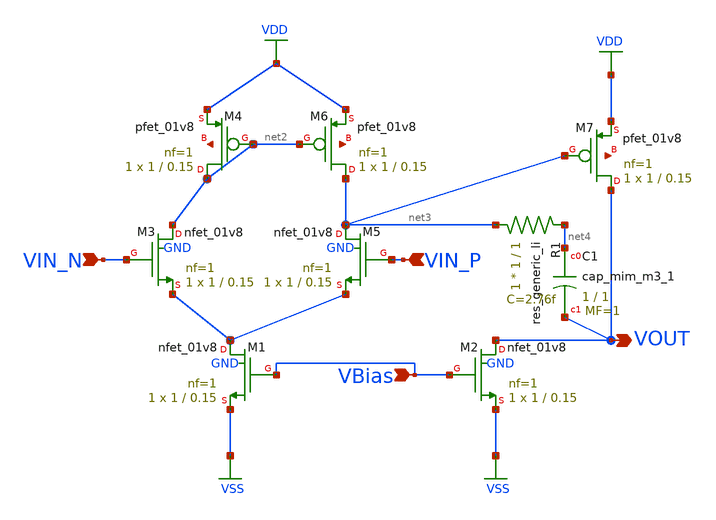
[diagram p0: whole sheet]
** sch_path: analog/schematics/bootcamp_opamp.sch
**.subckt bootcamp_opamp VIN_P VIN_N VOUT VBias
*.ipin VIN_P
*.ipin VIN_N
*.opin VOUT
*.ipin VBias
XM1 net1 VBias VSS GND sky130_fd_pr__nfet_01v8 L=0.15 W=1 nf=1 ad='int((nf+1)/2) * W/nf * 0.29' as='int((nf+2)/2) * W/nf * 0.29'
+ pd='2*int((nf+1)/2) * (W/nf + 0.29)' ps='2*int((nf+2)/2) * (W/nf + 0.29)' nrd='0.29 / W' nrs='0.29 / W'
+ sa=0 sb=0 sd=0 mult=1 m=1
XM2 VOUT VBias VSS GND sky130_fd_pr__nfet_01v8 L=0.15 W=1 nf=1 ad='int((nf+1)/2) * W/nf * 0.29' as='int((nf+2)/2) * W/nf * 0.29'
+ pd='2*int((nf+1)/2) * (W/nf + 0.29)' ps='2*int((nf+2)/2) * (W/nf + 0.29)' nrd='0.29 / W' nrs='0.29 / W'
+ sa=0 sb=0 sd=0 mult=1 m=1
XM3 net2 VIN_N net1 GND sky130_fd_pr__nfet_01v8 L=0.15 W=1 nf=1 ad='int((nf+1)/2) * W/nf * 0.29' as='int((nf+2)/2) * W/nf * 0.29'
+ pd='2*int((nf+1)/2) * (W/nf + 0.29)' ps='2*int((nf+2)/2) * (W/nf + 0.29)' nrd='0.29 / W' nrs='0.29 / W'
+ sa=0 sb=0 sd=0 mult=1 m=1
XM4 net2 net2 VDD net5 sky130_fd_pr__pfet_01v8 L=0.15 W=1 nf=1 ad='int((nf+1)/2) * W/nf * 0.29' as='int((nf+2)/2) * W/nf * 0.29'
+ pd='2*int((nf+1)/2) * (W/nf + 0.29)' ps='2*int((nf+2)/2) * (W/nf + 0.29)' nrd='0.29 / W' nrs='0.29 / W'
+ sa=0 sb=0 sd=0 mult=1 m=1
XM5 net3 VIN_P net1 GND sky130_fd_pr__nfet_01v8 L=0.15 W=1 nf=1 ad='int((nf+1)/2) * W/nf * 0.29' as='int((nf+2)/2) * W/nf * 0.29'
+ pd='2*int((nf+1)/2) * (W/nf + 0.29)' ps='2*int((nf+2)/2) * (W/nf + 0.29)' nrd='0.29 / W' nrs='0.29 / W'
+ sa=0 sb=0 sd=0 mult=1 m=1
XM6 net3 net2 VDD net6 sky130_fd_pr__pfet_01v8 L=0.15 W=1 nf=1 ad='int((nf+1)/2) * W/nf * 0.29' as='int((nf+2)/2) * W/nf * 0.29'
+ pd='2*int((nf+1)/2) * (W/nf + 0.29)' ps='2*int((nf+2)/2) * (W/nf + 0.29)' nrd='0.29 / W' nrs='0.29 / W'
+ sa=0 sb=0 sd=0 mult=1 m=1
XM7 VOUT net3 VDD net7 sky130_fd_pr__pfet_01v8 L=0.15 W=1 nf=1 ad='int((nf+1)/2) * W/nf * 0.29' as='int((nf+2)/2) * W/nf * 0.29'
+ pd='2*int((nf+1)/2) * (W/nf + 0.29)' ps='2*int((nf+2)/2) * (W/nf + 0.29)' nrd='0.29 / W' nrs='0.29 / W'
+ sa=0 sb=0 sd=0 mult=1 m=1
R1 net3 net4 sky130_fd_pr__res_generic_li W=1 L=1 m=1
XC1 net4 VOUT sky130_fd_pr__cap_mim_m3_1 W=1 L=1 MF=1 m=1
**.ends
.GLOBAL VDD
.GLOBAL VSS
.end
